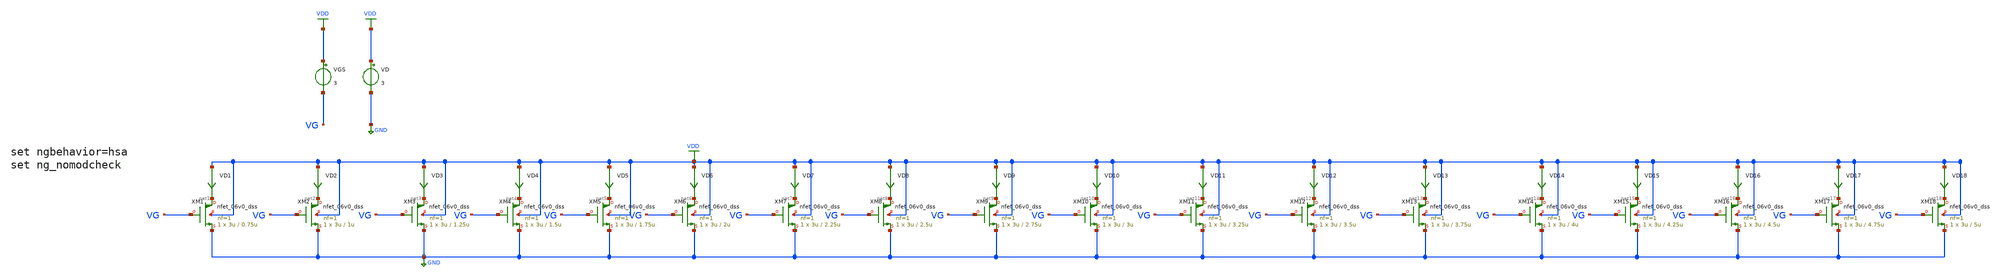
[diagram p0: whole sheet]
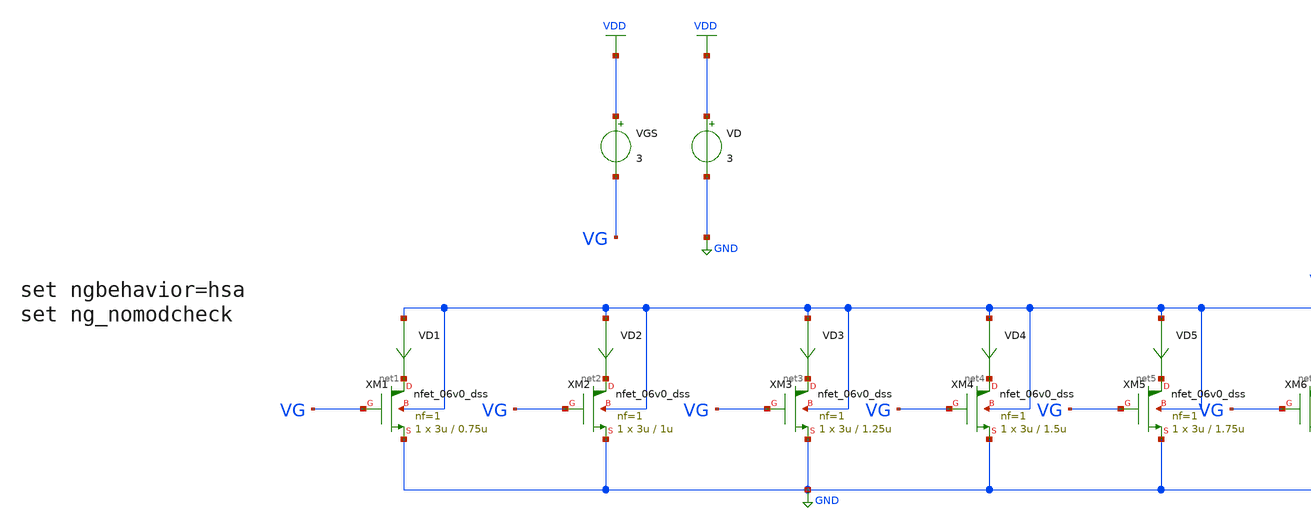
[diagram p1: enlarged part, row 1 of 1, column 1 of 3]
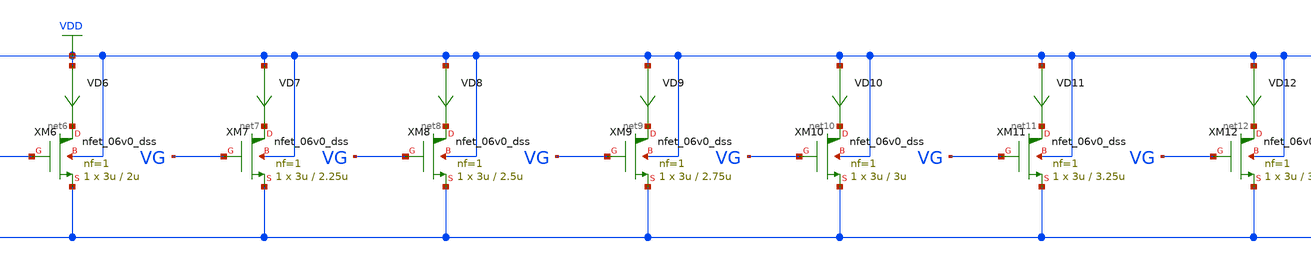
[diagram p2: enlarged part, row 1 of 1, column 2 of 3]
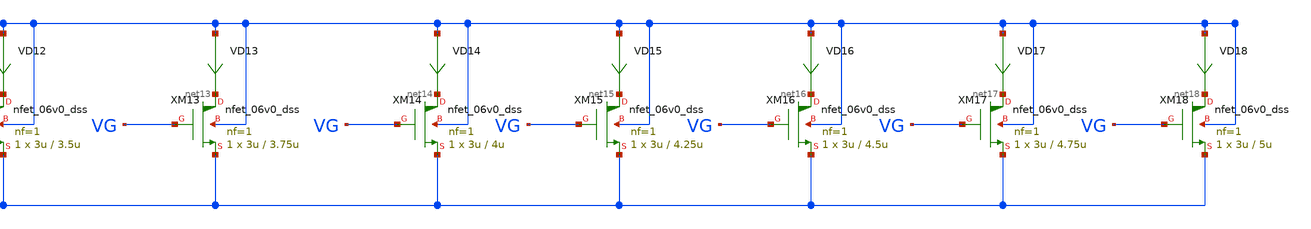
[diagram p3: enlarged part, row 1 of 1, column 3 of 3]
** sch_path: gmid Data/PMOS_06v0_SVT/PMOS_06v0_SVT/gmid_pmos_06v0_svt.sch
**.subckt gmid_pmos_06v0_svt
VGS VDD VG 3
VD VDD GND 3
VD1 VDD net1 0
.save i(vd1)
VD2 VDD net2 0
.save i(vd2)
VD3 VDD net3 0
.save i(vd3)
VD4 VDD net4 0
.save i(vd4)
VD5 VDD net5 0
.save i(vd5)
VD6 VDD net6 0
.save i(vd6)
VD7 VDD net7 0
.save i(vd7)
VD8 VDD net8 0
.save i(vd8)
VD9 VDD net9 0
.save i(vd9)
VD10 VDD net10 0
.save i(vd10)
VD11 VDD net11 0
.save i(vd11)
VD12 VDD net12 0
.save i(vd12)
VD13 VDD net13 0
.save i(vd13)
VD14 VDD net14 0
.save i(vd14)
VD15 VDD net15 0
.save i(vd15)
VD16 VDD net16 0
.save i(vd16)
VD17 VDD net17 0
.save i(vd17)
VD18 VDD net18 0
.save i(vd18)
XM1 net1 VG GND VDD nfet_06v0_dss L=0.75u W=3u nf=1 ad='int((nf+1)/2) * W/nf * 0.18u' as='int((nf+2)/2) * W/nf * 0.18u'
+ pd='2*int((nf+1)/2) * (W/nf + 0.18u)' ps='2*int((nf+2)/2) * (W/nf + 0.18u)' nrd='0.18u / W' nrs='0.18u / W'
+ sa=0 sb=0 sd=0 m=1
XM2 net2 VG GND VDD nfet_06v0_dss L=1u W=3u nf=1 ad='int((nf+1)/2) * W/nf * 0.18u' as='int((nf+2)/2) * W/nf * 0.18u'
+ pd='2*int((nf+1)/2) * (W/nf + 0.18u)' ps='2*int((nf+2)/2) * (W/nf + 0.18u)' nrd='0.18u / W' nrs='0.18u / W'
+ sa=0 sb=0 sd=0 m=1
XM3 net3 VG GND VDD nfet_06v0_dss L=1.25u W=3u nf=1 ad='int((nf+1)/2) * W/nf * 0.18u' as='int((nf+2)/2) * W/nf * 0.18u'
+ pd='2*int((nf+1)/2) * (W/nf + 0.18u)' ps='2*int((nf+2)/2) * (W/nf + 0.18u)' nrd='0.18u / W' nrs='0.18u / W'
+ sa=0 sb=0 sd=0 m=1
XM4 net4 VG GND VDD nfet_06v0_dss L=1.5u W=3u nf=1 ad='int((nf+1)/2) * W/nf * 0.18u' as='int((nf+2)/2) * W/nf * 0.18u'
+ pd='2*int((nf+1)/2) * (W/nf + 0.18u)' ps='2*int((nf+2)/2) * (W/nf + 0.18u)' nrd='0.18u / W' nrs='0.18u / W'
+ sa=0 sb=0 sd=0 m=1
XM5 net5 VG GND VDD nfet_06v0_dss L=1.75u W=3u nf=1 ad='int((nf+1)/2) * W/nf * 0.18u' as='int((nf+2)/2) * W/nf * 0.18u'
+ pd='2*int((nf+1)/2) * (W/nf + 0.18u)' ps='2*int((nf+2)/2) * (W/nf + 0.18u)' nrd='0.18u / W' nrs='0.18u / W'
+ sa=0 sb=0 sd=0 m=1
XM6 net6 VG GND VDD nfet_06v0_dss L=2u W=3u nf=1 ad='int((nf+1)/2) * W/nf * 0.18u' as='int((nf+2)/2) * W/nf * 0.18u'
+ pd='2*int((nf+1)/2) * (W/nf + 0.18u)' ps='2*int((nf+2)/2) * (W/nf + 0.18u)' nrd='0.18u / W' nrs='0.18u / W'
+ sa=0 sb=0 sd=0 m=1
XM7 net7 VG GND VDD nfet_06v0_dss L=2.25u W=3u nf=1 ad='int((nf+1)/2) * W/nf * 0.18u' as='int((nf+2)/2) * W/nf * 0.18u'
+ pd='2*int((nf+1)/2) * (W/nf + 0.18u)' ps='2*int((nf+2)/2) * (W/nf + 0.18u)' nrd='0.18u / W' nrs='0.18u / W'
+ sa=0 sb=0 sd=0 m=1
XM8 net8 VG GND VDD nfet_06v0_dss L=2.5u W=3u nf=1 ad='int((nf+1)/2) * W/nf * 0.18u' as='int((nf+2)/2) * W/nf * 0.18u'
+ pd='2*int((nf+1)/2) * (W/nf + 0.18u)' ps='2*int((nf+2)/2) * (W/nf + 0.18u)' nrd='0.18u / W' nrs='0.18u / W'
+ sa=0 sb=0 sd=0 m=1
XM9 net9 VG GND VDD nfet_06v0_dss L=2.75u W=3u nf=1 ad='int((nf+1)/2) * W/nf * 0.18u' as='int((nf+2)/2) * W/nf * 0.18u'
+ pd='2*int((nf+1)/2) * (W/nf + 0.18u)' ps='2*int((nf+2)/2) * (W/nf + 0.18u)' nrd='0.18u / W' nrs='0.18u / W'
+ sa=0 sb=0 sd=0 m=1
XM10 net10 VG GND VDD nfet_06v0_dss L=3u W=3u nf=1 ad='int((nf+1)/2) * W/nf * 0.18u' as='int((nf+2)/2) * W/nf * 0.18u'
+ pd='2*int((nf+1)/2) * (W/nf + 0.18u)' ps='2*int((nf+2)/2) * (W/nf + 0.18u)' nrd='0.18u / W' nrs='0.18u / W'
+ sa=0 sb=0 sd=0 m=1
XM11 net11 VG GND VDD nfet_06v0_dss L=3.25u W=3u nf=1 ad='int((nf+1)/2) * W/nf * 0.18u' as='int((nf+2)/2) * W/nf * 0.18u'
+ pd='2*int((nf+1)/2) * (W/nf + 0.18u)' ps='2*int((nf+2)/2) * (W/nf + 0.18u)' nrd='0.18u / W' nrs='0.18u / W'
+ sa=0 sb=0 sd=0 m=1
XM12 net12 VG GND VDD nfet_06v0_dss L=3.5u W=3u nf=1 ad='int((nf+1)/2) * W/nf * 0.18u' as='int((nf+2)/2) * W/nf * 0.18u'
+ pd='2*int((nf+1)/2) * (W/nf + 0.18u)' ps='2*int((nf+2)/2) * (W/nf + 0.18u)' nrd='0.18u / W' nrs='0.18u / W'
+ sa=0 sb=0 sd=0 m=1
XM13 net13 VG GND VDD nfet_06v0_dss L=3.75u W=3u nf=1 ad='int((nf+1)/2) * W/nf * 0.18u' as='int((nf+2)/2) * W/nf * 0.18u'
+ pd='2*int((nf+1)/2) * (W/nf + 0.18u)' ps='2*int((nf+2)/2) * (W/nf + 0.18u)' nrd='0.18u / W' nrs='0.18u / W'
+ sa=0 sb=0 sd=0 m=1
XM14 net14 VG GND VDD nfet_06v0_dss L=4u W=3u nf=1 ad='int((nf+1)/2) * W/nf * 0.18u' as='int((nf+2)/2) * W/nf * 0.18u'
+ pd='2*int((nf+1)/2) * (W/nf + 0.18u)' ps='2*int((nf+2)/2) * (W/nf + 0.18u)' nrd='0.18u / W' nrs='0.18u / W'
+ sa=0 sb=0 sd=0 m=1
XM15 net15 VG GND VDD nfet_06v0_dss L=4.25u W=3u nf=1 ad='int((nf+1)/2) * W/nf * 0.18u' as='int((nf+2)/2) * W/nf * 0.18u'
+ pd='2*int((nf+1)/2) * (W/nf + 0.18u)' ps='2*int((nf+2)/2) * (W/nf + 0.18u)' nrd='0.18u / W' nrs='0.18u / W'
+ sa=0 sb=0 sd=0 m=1
XM16 net16 VG GND VDD nfet_06v0_dss L=4.5u W=3u nf=1 ad='int((nf+1)/2) * W/nf * 0.18u' as='int((nf+2)/2) * W/nf * 0.18u'
+ pd='2*int((nf+1)/2) * (W/nf + 0.18u)' ps='2*int((nf+2)/2) * (W/nf + 0.18u)' nrd='0.18u / W' nrs='0.18u / W'
+ sa=0 sb=0 sd=0 m=1
XM17 net17 VG GND VDD nfet_06v0_dss L=4.75u W=3u nf=1 ad='int((nf+1)/2) * W/nf * 0.18u' as='int((nf+2)/2) * W/nf * 0.18u'
+ pd='2*int((nf+1)/2) * (W/nf + 0.18u)' ps='2*int((nf+2)/2) * (W/nf + 0.18u)' nrd='0.18u / W' nrs='0.18u / W'
+ sa=0 sb=0 sd=0 m=1
XM18 net18 VG GND VDD nfet_06v0_dss L=5u W=3u nf=1 ad='int((nf+1)/2) * W/nf * 0.18u' as='int((nf+2)/2) * W/nf * 0.18u'
+ pd='2*int((nf+1)/2) * (W/nf + 0.18u)' ps='2*int((nf+2)/2) * (W/nf + 0.18u)' nrd='0.18u / W' nrs='0.18u / W'
+ sa=0 sb=0 sd=0 m=1
**** begin user architecture code


.save @m.xm1.m0[gm]
.save @m.xm1.m0[vth]
.save @m.xm1.m0[gds]
.save @m.xm1.m0[cgg]
.save @m.xm1.m0[cgs]
.save @m.xm1.m0[cgd]
.save @m.xm2.m0[gm]
.save @m.xm2.m0[vth]
.save @m.xm2.m0[gds]
.save @m.xm2.m0[cgg]
.save @m.xm2.m0[cgs]
.save @m.xm2.m0[cgd]
.save @m.xm3.m0[gm]
.save @m.xm3.m0[vth]
.save @m.xm3.m0[gds]
.save @m.xm3.m0[cgg]
.save @m.xm3.m0[cgs]
.save @m.xm3.m0[cgd]
.save @m.xm4.m0[gm]
.save @m.xm4.m0[vth]
.save @m.xm4.m0[gds]
.save @m.xm4.m0[cgg]
.save @m.xm4.m0[cgs]
.save @m.xm4.m0[cgd]
.save @m.xm5.m0[gm]
.save @m.xm5.m0[vth]
.save @m.xm5.m0[gds]
.save @m.xm5.m0[cgg]
.save @m.xm5.m0[cgs]
.save @m.xm5.m0[cgd]
.save @m.xm6.m0[gm]
.save @m.xm6.m0[vth]
.save @m.xm6.m0[gds]
.save @m.xm6.m0[cgg]
.save @m.xm6.m0[cgs]
.save @m.xm6.m0[cgd]
.save @m.xm7.m0[gm]
.save @m.xm7.m0[vth]
.save @m.xm7.m0[gds]
.save @m.xm7.m0[cgg]
.save @m.xm7.m0[cgs]
.save @m.xm7.m0[cgd]
.save @m.xm8.m0[gm]
.save @m.xm8.m0[vth]
.save @m.xm8.m0[gds]
.save @m.xm8.m0[cgg]
.save @m.xm8.m0[cgs]
.save @m.xm8.m0[cgd]
.save @m.xm9.m0[gm]
.save @m.xm9.m0[vth]
.save @m.xm9.m0[gds]
.save @m.xm9.m0[cgg]
.save @m.xm9.m0[cgs]
.save @m.xm9.m0[cgd]
.save @m.xm10.m0[gm]
.save @m.xm10.m0[vth]
.save @m.xm10.m0[gds]
.save @m.xm10.m0[cgg]
.save @m.xm10.m0[cgs]
.save @m.xm10.m0[cgd]
.save @m.xm11.m0[gm]
.save @m.xm11.m0[vth]
.save @m.xm11.m0[gds]
.save @m.xm11.m0[cgg]
.save @m.xm11.m0[cgs]
.save @m.xm11.m0[cgd]
.save @m.xm12.m0[gm]
.save @m.xm12.m0[vth]
.save @m.xm12.m0[gds]
.save @m.xm12.m0[cgg]
.save @m.xm12.m0[cgs]
.save @m.xm12.m0[cgd]
.save @m.xm13.m0[gm]
.save @m.xm13.m0[vth]
.save @m.xm13.m0[gds]
.save @m.xm13.m0[cgg]
.save @m.xm13.m0[cgs]
.save @m.xm13.m0[cgd]
.save @m.xm14.m0[gm]
.save @m.xm14.m0[vth]
.save @m.xm14.m0[gds]
.save @m.xm14.m0[cgg]
.save @m.xm14.m0[cgs]
.save @m.xm14.m0[cgd]
.save @m.xm15.m0[gm]
.save @m.xm15.m0[vth]
.save @m.xm15.m0[gds]
.save @m.xm15.m0[cgg]
.save @m.xm15.m0[cgs]
.save @m.xm15.m0[cgd]
.save @m.xm16.m0[gm]
.save @m.xm16.m0[vth]
.save @m.xm16.m0[gds]
.save @m.xm16.m0[cgg]
.save @m.xm16.m0[cgs]
.save @m.xm16.m0[cgd]
.save @m.xm17.m0[gm]
.save @m.xm17.m0[vth]
.save @m.xm17.m0[gds]
.save @m.xm17.m0[cgg]
.save @m.xm17.m0[cgs]
.save @m.xm17.m0[cgd]
.save @m.xm18.m0[gm]
.save @m.xm18.m0[vth]
.save @m.xm18.m0[gds]
.save @m.xm18.m0[cgg]
.save @m.xm18.m0[cgs]
.save @m.xm18.m0[cgd]





.lib /foss/pdks/volare/gf180mcu/versions/0fe599b2afb6708d281543108caf8310912f54af/gf180mcuD/libs.tech/ngspice/sm141064.ngspice typical
.include /foss/pdks/volare/gf180mcu/versions/0fe599b2afb6708d281543108caf8310912f54af/gf180mcuD/libs.tech/ngspice/design.ngspice

*.include $::180MCU_MODELS/design.ngspice
*.lib $::180MCU_MODELS/sm141064.ngspice typical




* ngspice commands
.option wnflag=1
.option .savecurrents
.control
save all
dc VGS 0.05 6 0.1m
** remove zero length vectors to prevent write errors
remzerovec
write /foss/designs/PDK-CHAR/GF180-MCUD/PMOS_06v0_SVT/gmid_PMOS_06v0_SVT_tb.raw

plot @m.xm1.m0[gm]
plot @m.xm2.m0[gm]
plot @m.xm3.m0[gm]
plot @m.xm4.m0[gm]
plot @m.xm5.m0[gm]
plot @m.xm6.m0[gm]
plot @m.xm7.m0[gm]
plot @m.xm8.m0[gm]
plot @m.xm9.m0[gm]
plot @m.xm10.m0[gm]
plot @m.xm11.m0[gm]
plot @m.xm12.m0[gm]
plot @m.xm13.m0[gm]
plot @m.xm14.m0[gm]
plot @m.xm15.m0[gm]
plot @m.xm16.m0[gm]
plot @m.xm17.m0[gm]
plot @m.xm18.m0[gm]
*plot @m.xm19.m0[gm]

wrdata /foss/designs/PDK-CHAR/GF180-MCUD/PMOS_06v0_SVT/gmid_pmos_1_pfet_06v0_svt_tb.txt
+ @m.xm1.m0[gm] i(VD1) @m.xm1.m0[vth] @m.xm1.m0[gds] @m.xm1.m0[cgg] @m.xm1.m0[cgs] @m.xm1.m0[cgd]
wrdata /foss/designs/PDK-CHAR/GF180-MCUD/PMOS_06v0_SVT/gmid_pmos_2_pfet_06v0_svt_tb.txt
+ @m.xm2.m0[gm] i(VD2) @m.xm2.m0[vth] @m.xm2.m0[gds] @m.xm2.m0[cgg] @m.xm2.m0[cgs] @m.xm2.m0[cgd]
wrdata /foss/designs/PDK-CHAR/GF180-MCUD/PMOS_06v0_SVT/gmid_pmos_3_pfet_06v0_svt_tb.txt
+ @m.xm3.m0[gm] i(VD3) @m.xm3.m0[vth] @m.xm3.m0[gds] @m.xm3.m0[cgg] @m.xm3.m0[cgs] @m.xm3.m0[cgd]
wrdata /foss/designs/PDK-CHAR/GF180-MCUD/PMOS_06v0_SVT/gmid_pmos_4_pfet_06v0_svt_tb.txt
+ @m.xm4.m0[gm] i(VD4) @m.xm4.m0[vth] @m.xm4.m0[gds] @m.xm4.m0[cgg] @m.xm4.m0[cgs] @m.xm4.m0[cgd]
wrdata /foss/designs/PDK-CHAR/GF180-MCUD/PMOS_06v0_SVT/gmid_pmos_5_pfet_06v0_svt_tb.txt
+ @m.xm5.m0[gm] i(VD5) @m.xm5.m0[vth] @m.xm5.m0[gds] @m.xm5.m0[cgg] @m.xm5.m0[cgs] @m.xm5.m0[cgd]
wrdata /foss/designs/PDK-CHAR/GF180-MCUD/PMOS_06v0_SVT/gmid_pmos_6_pfet_06v0_svt_tb.txt
+ @m.xm6.m0[gm] i(VD6) @m.xm6.m0[vth] @m.xm6.m0[gds] @m.xm6.m0[cgg] @m.xm6.m0[cgs] @m.xm6.m0[cgd]
wrdata /foss/designs/PDK-CHAR/GF180-MCUD/PMOS_06v0_SVT/gmid_pmos_7_pfet_06v0_svt_tb.txt
+ @m.xm7.m0[gm] i(VD7) @m.xm7.m0[vth] @m.xm7.m0[gds] @m.xm7.m0[cgg] @m.xm7.m0[cgs] @m.xm7.m0[cgd]
wrdata /foss/designs/PDK-CHAR/GF180-MCUD/PMOS_06v0_SVT/gmid_pmos_8_pfet_06v0_svt_tb.txt
+ @m.xm8.m0[gm] i(VD8) @m.xm8.m0[vth] @m.xm8.m0[gds] @m.xm8.m0[cgg] @m.xm8.m0[cgs] @m.xm8.m0[cgd]
wrdata /foss/designs/PDK-CHAR/GF180-MCUD/PMOS_06v0_SVT/gmid_pmos_9_pfet_06v0_svt_tb.txt
+ @m.xm9.m0[gm] i(VD9) @m.xm9.m0[vth] @m.xm9.m0[gds] @m.xm9.m0[cgg] @m.xm9.m0[cgs] @m.xm9.m0[cgd]
wrdata /foss/designs/PDK-CHAR/GF180-MCUD/PMOS_06v0_SVT/gmid_pmos_10_pfet_06v0_svt_tb.txt
+ @m.xm10.m0[gm] i(VD10) @m.xm10.m0[vth] @m.xm10.m0[gds] @m.xm10.m0[cgg] @m.xm10.m0[cgs] @m.xm10.m0[cgd]
wrdata /foss/designs/PDK-CHAR/GF180-MCUD/PMOS_06v0_SVT/gmid_pmos_11_pfet_06v0_svt_tb.txt
+ @m.xm11.m0[gm] i(VD11) @m.xm11.m0[vth] @m.xm11.m0[gds] @m.xm11.m0[cgg] @m.xm11.m0[cgs] @m.xm11.m0[cgd]
wrdata /foss/designs/PDK-CHAR/GF180-MCUD/PMOS_06v0_SVT/gmid_pmos_12_pfet_06v0_svt_tb.txt
+ @m.xm12.m0[gm] i(VD12) @m.xm12.m0[vth] @m.xm12.m0[gds] @m.xm12.m0[cgg] @m.xm12.m0[cgs] @m.xm12.m0[cgd]
wrdata /foss/designs/PDK-CHAR/GF180-MCUD/PMOS_06v0_SVT/gmid_pmos_13_pfet_06v0_svt_tb.txt
+ @m.xm13.m0[gm] i(VD13) @m.xm13.m0[vth] @m.xm13.m0[gds] @m.xm13.m0[cgg] @m.xm13.m0[cgs] @m.xm13.m0[cgd]
wrdata /foss/designs/PDK-CHAR/GF180-MCUD/PMOS_06v0_SVT/gmid_pmos_14_pfet_06v0_svt_tb.txt
+ @m.xm14.m0[gm] i(VD14) @m.xm14.m0[vth] @m.xm14.m0[gds] @m.xm14.m0[cgg] @m.xm14.m0[cgs] @m.xm14.m0[cgd]
wrdata /foss/designs/PDK-CHAR/GF180-MCUD/PMOS_06v0_SVT/gmid_pmos_15_pfet_06v0_svt_tb.txt
+ @m.xm15.m0[gm] i(VD15) @m.xm15.m0[vth] @m.xm15.m0[gds] @m.xm15.m0[cgg] @m.xm15.m0[cgs] @m.xm15.m0[cgd]
wrdata /foss/designs/PDK-CHAR/GF180-MCUD/PMOS_06v0_SVT/gmid_pmos_16_pfet_06v0_svt_tb.txt
+ @m.xm16.m0[gm] i(VD16) @m.xm16.m0[vth] @m.xm16.m0[gds] @m.xm16.m0[cgg] @m.xm16.m0[cgs] @m.xm16.m0[cgd]
wrdata /foss/designs/PDK-CHAR/GF180-MCUD/PMOS_06v0_SVT/gmid_pmos_17_pfet_06v0_svt_tb.txt
+ @m.xm17.m0[gm] i(VD17) @m.xm17.m0[vth] @m.xm17.m0[gds] @m.xm17.m0[cgg] @m.xm17.m0[cgs] @m.xm17.m0[cgd]
wrdata /foss/designs/PDK-CHAR/GF180-MCUD/PMOS_06v0_SVT/gmid_pmos_18_pfet_06v0_svt_tb.txt
+ @m.xm18.m0[gm] i(VD18) @m.xm18.m0[vth] @m.xm18.m0[gds] @m.xm18.m0[cgg] @m.xm18.m0[cgs] @m.xm18.m0[cgd]
*wrdata /foss/designs/PDK-CHAR/GF180-MCUD/PMOS_06v0_SVT/gmid_pmos_19_pfet_06v0_svt_tb.txt
*+ @m.xm19.m0[gm] i(VD19) @m.xm19.m0[vth] @m.xm19.m0[gds] @m.xm19.m0[cgg] @m.xm19.m0[cgs] @m.xm19.m0[cgd]
set appendwrite
op
remzerovec
write /foss/designs/PDK-CHAR/GF180-MCUD/PMOS_06v0_SVT/gmid_PMOS_06v0_SVT_tb.raw
**quit 0
.endc


**** end user architecture code
**.ends
.GLOBAL GND
.GLOBAL VDD
.end
